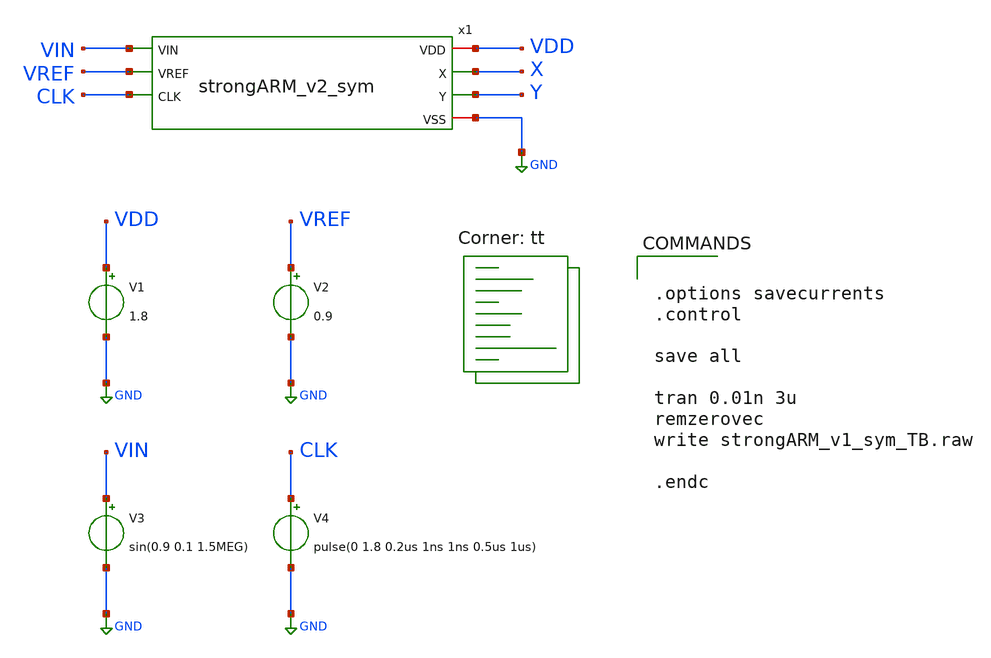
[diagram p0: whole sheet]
** sch_path: strongARM/strongARM_v1_sym_TB.sch
**.subckt strongARM_v1_sym_TB
V1 VDD GND 1.8
V3 VIN GND sin(0.9 0.1 1.5MEG)
V2 VREF GND 0.9
V4 CLK GND pulse(0 1.8 0.2us 1ns 1ns 0.5us 1us)
x1 VDD X Y VIN VREF CLK GND strongARM_v2_sym
**** begin user architecture code
.lib $::SKYWATER_MODELS/sky130.lib.spice tt


.options savecurrents
.control

save all

tran 0.01n 3u
remzerovec
write strongARM_v1_sym_TB.raw

.endc


**** end user architecture code
**.ends

* expanding   symbol:  /foss/designs/Analog_FA23_SP24/strongARM/strongARM_v2_sym.sym # of pins=7
** sym_path: strongARM/strongARM_v2_sym.sym
** sch_path: strongARM/strongARM_v2_sym.sch
.subckt strongARM_v2_sym VDD X Y VIN VREF CLK VSS
*.iopin VDD
*.ipin VIN
*.ipin VREF
*.opin Y
*.opin X
*.iopin VSS
*.ipin CLK
XM4 net2 CLK VDD VDD sky130_fd_pr__pfet_01v8_lvt L=0.35 W=1 nf=1 ad='int((nf+1)/2) * W/nf * 0.29' as='int((nf+2)/2) * W/nf * 0.29'
+ pd='2*int((nf+1)/2) * (W/nf + 0.29)' ps='2*int((nf+2)/2) * (W/nf + 0.29)' nrd='0.29 / W' nrs='0.29 / W'
+ sa=0 sb=0 sd=0 mult=1 m=1
XM1 X CLK VDD VDD sky130_fd_pr__pfet_01v8_lvt L=0.35 W=1 nf=1 ad='int((nf+1)/2) * W/nf * 0.29' as='int((nf+2)/2) * W/nf * 0.29'
+ pd='2*int((nf+1)/2) * (W/nf + 0.29)' ps='2*int((nf+2)/2) * (W/nf + 0.29)' nrd='0.29 / W' nrs='0.29 / W'
+ sa=0 sb=0 sd=0 mult=1 m=1
XM2 Y X VDD VDD sky130_fd_pr__pfet_01v8_lvt L=0.35 W=1 nf=1 ad='int((nf+1)/2) * W/nf * 0.29' as='int((nf+2)/2) * W/nf * 0.29'
+ pd='2*int((nf+1)/2) * (W/nf + 0.29)' ps='2*int((nf+2)/2) * (W/nf + 0.29)' nrd='0.29 / W' nrs='0.29 / W'
+ sa=0 sb=0 sd=0 mult=1 m=1
XM3 X Y VDD VDD sky130_fd_pr__pfet_01v8_lvt L=0.35 W=1 nf=1 ad='int((nf+1)/2) * W/nf * 0.29' as='int((nf+2)/2) * W/nf * 0.29'
+ pd='2*int((nf+1)/2) * (W/nf + 0.29)' ps='2*int((nf+2)/2) * (W/nf + 0.29)' nrd='0.29 / W' nrs='0.29 / W'
+ sa=0 sb=0 sd=0 mult=1 m=1
XM5 Y CLK VDD VDD sky130_fd_pr__pfet_01v8_lvt L=0.35 W=1 nf=1 ad='int((nf+1)/2) * W/nf * 0.29' as='int((nf+2)/2) * W/nf * 0.29'
+ pd='2*int((nf+1)/2) * (W/nf + 0.29)' ps='2*int((nf+2)/2) * (W/nf + 0.29)' nrd='0.29 / W' nrs='0.29 / W'
+ sa=0 sb=0 sd=0 mult=1 m=1
XM6 net3 CLK VDD VDD sky130_fd_pr__pfet_01v8_lvt L=0.35 W=1 nf=1 ad='int((nf+1)/2) * W/nf * 0.29' as='int((nf+2)/2) * W/nf * 0.29'
+ pd='2*int((nf+1)/2) * (W/nf + 0.29)' ps='2*int((nf+2)/2) * (W/nf + 0.29)' nrd='0.29 / W' nrs='0.29 / W'
+ sa=0 sb=0 sd=0 mult=1 m=1
XM10 X Y net2 VSS sky130_fd_pr__nfet_01v8_lvt L=0.15 W=1 nf=1 ad='int((nf+1)/2) * W/nf * 0.29' as='int((nf+2)/2) * W/nf * 0.29'
+ pd='2*int((nf+1)/2) * (W/nf + 0.29)' ps='2*int((nf+2)/2) * (W/nf + 0.29)' nrd='0.29 / W' nrs='0.29 / W'
+ sa=0 sb=0 sd=0 mult=1 m=1
XM7 Y X net3 VSS sky130_fd_pr__nfet_01v8_lvt L=0.15 W=1 nf=1 ad='int((nf+1)/2) * W/nf * 0.29' as='int((nf+2)/2) * W/nf * 0.29'
+ pd='2*int((nf+1)/2) * (W/nf + 0.29)' ps='2*int((nf+2)/2) * (W/nf + 0.29)' nrd='0.29 / W' nrs='0.29 / W'
+ sa=0 sb=0 sd=0 mult=1 m=1
XM8 net2 VIN net1 VSS sky130_fd_pr__nfet_01v8_lvt L=0.15 W=4 nf=1 ad='int((nf+1)/2) * W/nf * 0.29' as='int((nf+2)/2) * W/nf * 0.29'
+ pd='2*int((nf+1)/2) * (W/nf + 0.29)' ps='2*int((nf+2)/2) * (W/nf + 0.29)' nrd='0.29 / W' nrs='0.29 / W'
+ sa=0 sb=0 sd=0 mult=6 m=6
XM9 net3 VREF net1 VSS sky130_fd_pr__nfet_01v8_lvt L=0.15 W=4 nf=1 ad='int((nf+1)/2) * W/nf * 0.29' as='int((nf+2)/2) * W/nf * 0.29'
+ pd='2*int((nf+1)/2) * (W/nf + 0.29)' ps='2*int((nf+2)/2) * (W/nf + 0.29)' nrd='0.29 / W' nrs='0.29 / W'
+ sa=0 sb=0 sd=0 mult=6 m=6
XM11 net1 CLK VSS VSS sky130_fd_pr__nfet_01v8_lvt L=0.15 W=4 nf=1 ad='int((nf+1)/2) * W/nf * 0.29' as='int((nf+2)/2) * W/nf * 0.29'
+ pd='2*int((nf+1)/2) * (W/nf + 0.29)' ps='2*int((nf+2)/2) * (W/nf + 0.29)' nrd='0.29 / W' nrs='0.29 / W'
+ sa=0 sb=0 sd=0 mult=12 m=12
.ends

.GLOBAL GND
.end
